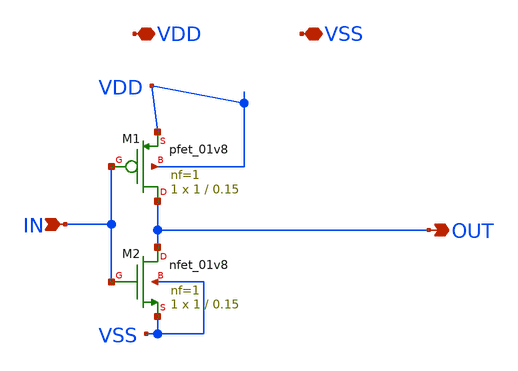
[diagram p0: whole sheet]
** sch_path: xschem/gilbert_mixer.sch
**.subckt gilbert_mixer VDD VSS OUT IN
*.iopin VDD
*.iopin VSS
*.opin OUT
*.ipin IN
XM1 OUT IN VDD VDD sky130_fd_pr__pfet_01v8 L=0.15 W=1 nf=1 ad='int((nf+1)/2) * W/nf * 0.29' as='int((nf+2)/2) * W/nf * 0.29'
+ pd='2*int((nf+1)/2) * (W/nf + 0.29)' ps='2*int((nf+2)/2) * (W/nf + 0.29)' nrd='0.29 / W' nrs='0.29 / W'
+ sa=0 sb=0 sd=0 mult=1 m=1
XM2 OUT IN VSS VSS sky130_fd_pr__nfet_01v8 L=0.15 W=1 nf=1 ad='int((nf+1)/2) * W/nf * 0.29' as='int((nf+2)/2) * W/nf * 0.29'
+ pd='2*int((nf+1)/2) * (W/nf + 0.29)' ps='2*int((nf+2)/2) * (W/nf + 0.29)' nrd='0.29 / W' nrs='0.29 / W'
+ sa=0 sb=0 sd=0 mult=1 m=1
**.ends
.end
